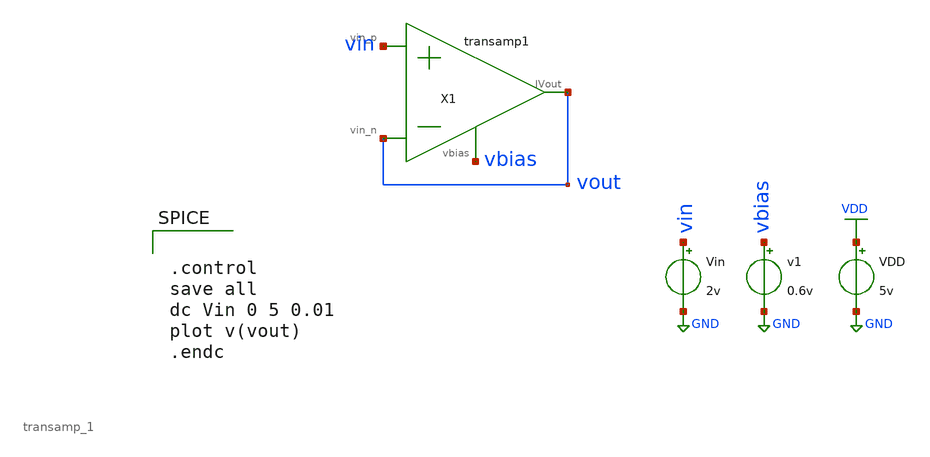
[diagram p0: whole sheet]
** sch_path: schematics/transamp_1_tb.sch
**.subckt transamp_1_tb
VDD VDD GND 5v
X1 vin vout vout vbias transamp_1
v1 vbias GND 0.6v
Vin vin GND 2v
**** begin user architecture code


.control
save all
dc Vin 0 5 0.01
plot v(vout)
.endc


 .lib $::SKYWATER_MODELS/models/sky130.lib.spice tt

.param mc_mm_switch=0
.param mc_pr_switch=1

**** end user architecture code
**.ends

* expanding   symbol:  /media/sf_share/circuitexamples/transamp_1.sym # of pins=4
** sym_path: schematics/transamp_1.sym
** sch_path: schematics/transamp_1.sch
.subckt transamp_1 vin_p vin_n IVout vbias
*.opin IVout
*.ipin vin_p
*.ipin vin_n
*.ipin vbias
XM1 net1 vbias GND GND sky130_fd_pr__nfet_g5v0d10v5 L=1 W=1 nf=1 ad='int((nf+1)/2) * W/nf * 0.29' as='int((nf+2)/2) * W/nf * 0.29'
+ pd='2*int((nf+1)/2) * (W/nf + 0.29)' ps='2*int((nf+2)/2) * (W/nf + 0.29)' nrd='0.29 / W' nrs='0.29 / W'
+ sa=0 sb=0 sd=0 mult=1 m=1
XM3 net2 vin_p net1 GND sky130_fd_pr__nfet_g5v0d10v5 L=1 W=1 nf=1 ad='int((nf+1)/2) * W/nf * 0.29' as='int((nf+2)/2) * W/nf * 0.29'
+ pd='2*int((nf+1)/2) * (W/nf + 0.29)' ps='2*int((nf+2)/2) * (W/nf + 0.29)' nrd='0.29 / W' nrs='0.29 / W'
+ sa=0 sb=0 sd=0 mult=1 m=1
XM4 IVout net2 VDD VDD sky130_fd_pr__pfet_g5v0d10v5 L=1 W=1 nf=1 ad='int((nf+1)/2) * W/nf * 0.29' as='int((nf+2)/2) * W/nf * 0.29'
+ pd='2*int((nf+1)/2) * (W/nf + 0.29)' ps='2*int((nf+2)/2) * (W/nf + 0.29)' nrd='0.29 / W' nrs='0.29 / W'
+ sa=0 sb=0 sd=0 mult=1 m=1
XM2 IVout vin_n net1 GND sky130_fd_pr__nfet_g5v0d10v5 L=1 W=1 nf=1 ad='int((nf+1)/2) * W/nf * 0.29' as='int((nf+2)/2) * W/nf * 0.29'
+ pd='2*int((nf+1)/2) * (W/nf + 0.29)' ps='2*int((nf+2)/2) * (W/nf + 0.29)' nrd='0.29 / W' nrs='0.29 / W'
+ sa=0 sb=0 sd=0 mult=1 m=1
XM5 net2 net2 VDD VDD sky130_fd_pr__pfet_g5v0d10v5 L=1 W=1 nf=1 ad='int((nf+1)/2) * W/nf * 0.29' as='int((nf+2)/2) * W/nf * 0.29'
+ pd='2*int((nf+1)/2) * (W/nf + 0.29)' ps='2*int((nf+2)/2) * (W/nf + 0.29)' nrd='0.29 / W' nrs='0.29 / W'
+ sa=0 sb=0 sd=0 mult=1 m=1
.ends

.GLOBAL VDD
.GLOBAL GND
.end
